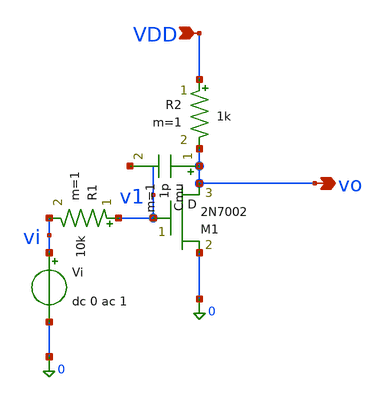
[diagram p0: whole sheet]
** sch_path: xschem_libraries_oa/SANDBOX/cs_amp.sch
**.subckt cs_amp VDD vo
*.ipin VDD
*.opin vo
M1 vo v1 0 M2N7002 m=1
R1 v1 vi 10k m=1
R2 VDD vo 1k m=1
Cmu vo v1 1p m=1
Vi vi 0 dc 0 ac 1
**.ends
.end
